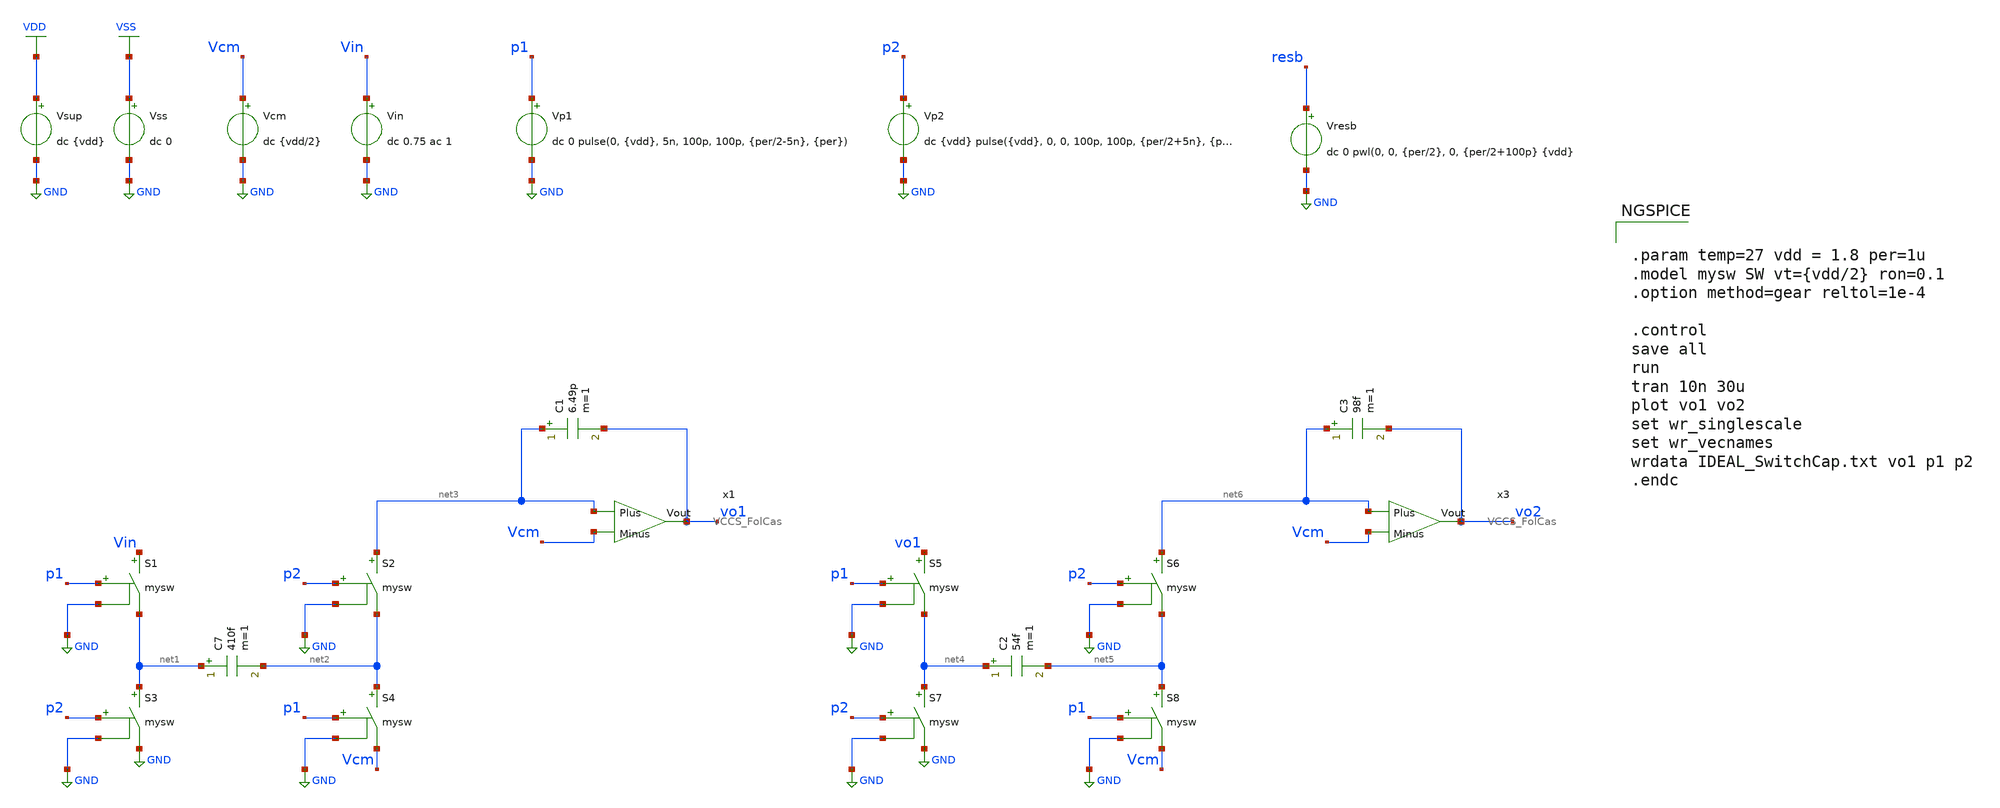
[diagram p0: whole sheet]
** sch_path: DSM/IC_Designs_Hrishi/RealCircuits/RealSwitchCap_FolCas.sch
* DSM/Schematics/IC_Designs_Hrishi/RealCircuits/Folded Cascode/FoldedCascodeOTA.sch:
* (c) 2024 Hrishikesh, @HSB
**.subckt RealSwitchCap_FolCas
Vcm Vcm GND dc {vdd/2}
Vin Vin GND dc 0.75 ac 1
Vp1 p1 GND dc 0 pulse(0, {vdd}, 5n, 100p, 100p, {per/2-5n}, {per})
Vp2 p2 GND dc {vdd} pulse({vdd}, 0, 0, 100p, 100p, {per/2+5n}, {per})
S1 Vin net1 p1 GND mysw
S2 net3 net2 p2 GND mysw
S3 net1 GND p2 GND mysw
S4 net2 Vcm p1 GND mysw
C7 net1 net2 410f m=1
C1 net3 vo1 6.49p m=1
Vresb resb GND dc 0 pwl(0, 0, {per/2}, 0, {per/2+100p} {vdd}
Vsup VDD GND dc {vdd}
Vss VSS GND dc 0
S5 vo1 net4 p1 GND mysw
S6 net6 net5 p2 GND mysw
S7 net4 GND p2 GND mysw
S8 net5 Vcm p1 GND mysw
C2 net4 net5 54f m=1
C3 net6 vo2 98f m=1
x1 net3 vo1 Vcm VCCS_FolCas
x3 net6 vo2 Vcm VCCS_FolCas
**** begin user architecture code

.lib $::SG13G2_MODELS/cornerMOSlv.lib mos_tt
.lib $::SG13G2_MODELS/cornerRES.lib res_typ
.inc /foss/pdks/sg13g2/libs.ref/sg13g2_stdcell/spice/sg13g2_stdcell.spice



.param temp=27 vdd = 1.8 per=1u
.model mysw SW vt={vdd/2} ron=0.1
.option method=gear reltol=1e-4

.control
save all
run
tran 10n 30u
plot vo1 vo2
set wr_singlescale
set wr_vecnames
wrdata IDEAL_SwitchCap.txt vo1 p1 p2
.endc


**** end user architecture code
**.ends

* expanding   symbol:
*+  /foss/designs/SecondOrder_SingleBit_DSM/DSM/IC_Designs_Hrishi/RealCircuits/VCCS_FolCas.sym # of pins=3
** sym_path: DSM/Schematics/Designs_Hrishi/RealCircuits/VCCS_FolCas.sym
** sch_path: DSM/Schematics/Designs_Hrishi/RealCircuits/VCCS_FolCas.sch
.subckt VCCS_FolCas Plus Vout Minus
*.ipin Minus
*.opin Vout
*.ipin Plus
Vdd v_dd GND 1.5
Vss v_ss GND 0
I0 v_dd net1 0.8u
x1 v_dd net1 Plus Minus Vout v_ss FoldedCascodeOTA
.ends


* expanding   symbol:  /foss/designs/CEMS_DSM/DSM/Schematics/IC_Designs_Hrishi/RealCircuits/Folded
*+ Cascode/FoldedCascodeOTA.sym # of pins=6
** sym_path: DSM/Schematics/IC_Designs_Hrishi/RealCircuits/Folded Cascode/FoldedCascodeOTA.sym
** sch_path: DSM/Schematics/IC_Designs_Hrishi/RealCircuits/Folded Cascode/FoldedCascodeOTA.sch
.subckt FoldedCascodeOTA VDD I PLUS MINUS Vout VSS
*.ipin PLUS
*.ipin MINUS
*.opin Vout
*.ipin VDD
*.ipin VSS
*.ipin I
XM1 net2 net4 VDD VDD sg13_lv_pmos w=0.272u l=0.5u ng=1 m=1 mm_ok=1
XM2 net1 PLUS net2 VDD sg13_lv_pmos w=0.136u l=0.5u ng=1 m=1 mm_ok=1
XM3 net6 MINUS net2 VDD sg13_lv_pmos w=0.136u l=0.5u ng=1 m=1 mm_ok=1
XM14 net6 net9 VSS VSS sg13_lv_nmos w=0.30u l=2u ng=1 m=1 mm_ok=1
XM13 Vout I net6 VSS sg13_lv_nmos w=0.15u l=2u ng=1 m=1 mm_ok=1
XM11 net7 I net1 VSS sg13_lv_nmos w=0.15u l=2u ng=1 m=1 mm_ok=1
XM12 net1 net9 VSS VSS sg13_lv_nmos w=0.30u l=2u ng=1 m=1 mm_ok=1
XM5 Vout net3 net5 VDD sg13_lv_pmos w=0.136u l=0.5u ng=1 m=1 mm_ok=1
XM4 net5 net4 VDD VDD sg13_lv_pmos w=0.136u l=0.5u ng=1 m=1 mm_ok=1
XM6 net4 net4 VDD VDD sg13_lv_pmos w=0.136u l=0.5u ng=1 m=1 mm_ok=1
XM8 net3 net3 net4 VDD sg13_lv_pmos w=0.136u l=0.5u ng=1 m=1 mm_ok=1
XM9 net8 net4 VDD VDD sg13_lv_pmos w=0.136u l=0.5u ng=1 m=1 mm_ok=1
XM10 net7 net3 net8 VDD sg13_lv_pmos w=0.136u l=0.5u ng=1 m=1 mm_ok=1
XM16 I I net9 VSS sg13_lv_nmos w=0.15u l=2u ng=1 m=1 mm_ok=1
XM15 net9 net9 VSS VSS sg13_lv_nmos w=0.15u l=2u ng=1 m=1 mm_ok=1
XM7 net3 net9 VSS VSS sg13_lv_nmos w=0.15u l=2u ng=1 m=1 mm_ok=1
XM18 VDD I net10 VSS sg13_lv_nmos w=0.15u l=2u ng=1 m=1 mm_ok=1
XM17 net10 net9 VSS VSS sg13_lv_nmos w=0.15u l=2u ng=1 m=1 mm_ok=1
.ends

.GLOBAL GND
.GLOBAL VDD
.GLOBAL VSS
.end
